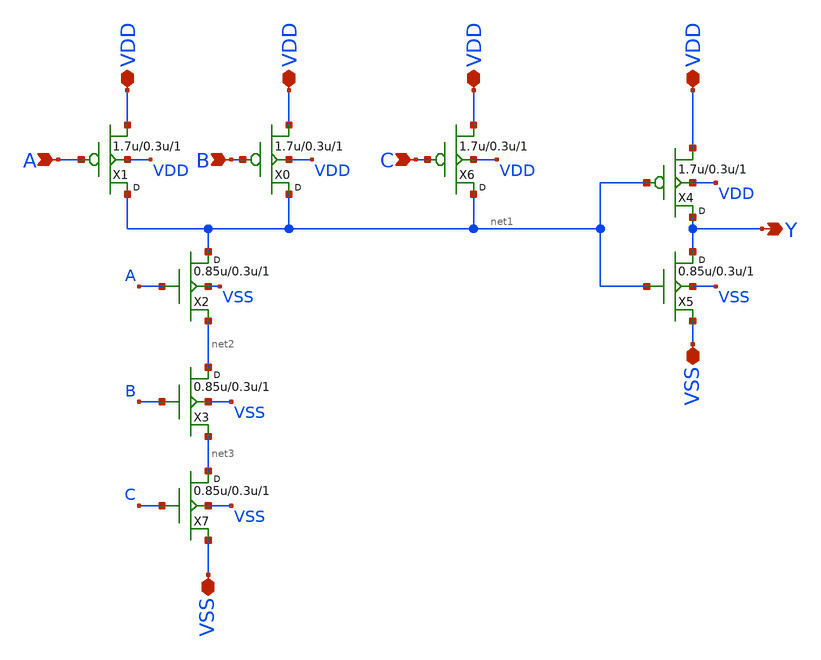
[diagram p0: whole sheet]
** sch_path: designs/libs/core_digital/gf180mcu_osu_sc_gp12t3v3/cells/and3/xschem/gf180mcu_osu_sc_gp12t3v3_and3_1.sch
**.subckt gf180mcu_osu_sc_gp12t3v3_and3_1 A B Y C VDD VDD VDD VDD VSS VSS
*.ipin A
*.ipin B
*.opin Y
*.ipin C
*.iopin VDD
*.iopin VDD
*.iopin VDD
*.iopin VDD
*.iopin VSS
*.iopin VSS
X1 net1 A VDD VDD pfet_03v3 w=1.7u l=0.3u m=1
X0 net1 B VDD VDD pfet_03v3 w=1.7u l=0.3u m=1
X2 net1 A net2 VSS nfet_03v3 w=0.85u l=0.3u m=1
X3 net2 B net3 VSS nfet_03v3 w=0.85u l=0.3u m=1
X4 Y net1 VDD VDD pfet_03v3 w=1.7u l=0.3u m=1
X5 Y net1 VSS VSS nfet_03v3 w=0.85u l=0.3u m=1
X6 net1 C VDD VDD pfet_03v3 w=1.7u l=0.3u m=1
X7 net3 C VSS VSS nfet_03v3 w=0.85u l=0.3u m=1
**.ends
.end
